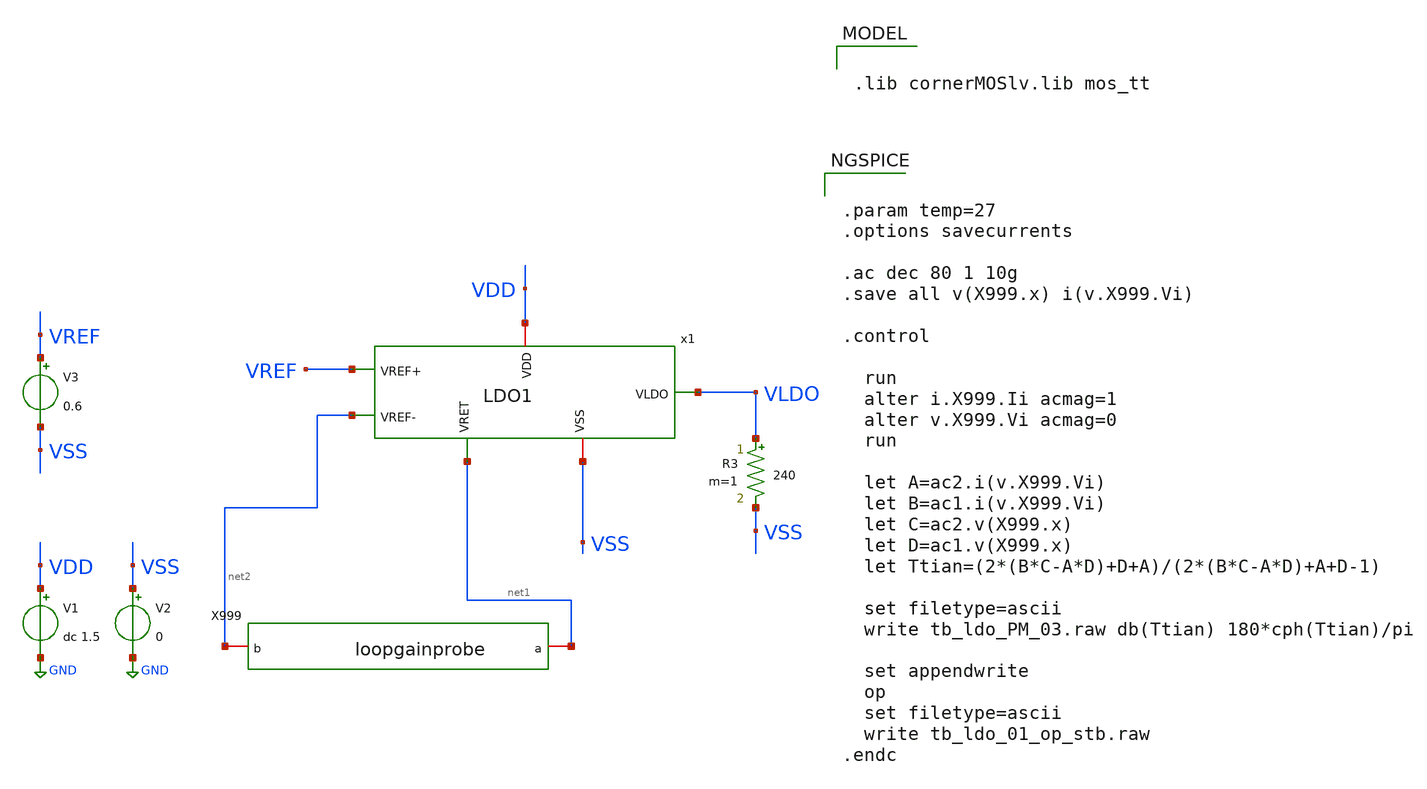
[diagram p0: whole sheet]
** sch_path: designs/1iee34/tb_ldo_PM.sch
**.subckt tb_ldo_PM
V1 VDD GND dc 1.5
V2 VSS GND 0
V3 VREF VSS 0.6
R3 VLDO VSS 240 m=1
x1 VDD VREF net2 VLDO net1 VSS LDO1
X999 net2 net1 loopgainprobe
**** begin user architecture code


.param temp=27
.options savecurrents

.ac dec 80 1 10g
.save all v(X999.x) i(v.X999.Vi)

.control

  run
  alter i.X999.Ii acmag=1
  alter v.X999.Vi acmag=0
  run

  let A=ac2.i(v.X999.Vi)
  let B=ac1.i(v.X999.Vi)
  let C=ac2.v(X999.x)
  let D=ac1.v(X999.x)
  let Ttian=(2*(B*C-A*D)+D+A)/(2*(B*C-A*D)+A+D-1)

  set filetype=ascii
  write tb_ldo_PM_03.raw db(Ttian) 180*cph(Ttian)/pi

  set appendwrite
  op
  set filetype=ascii
  write tb_ldo_01_op_stb.raw
.endc




.lib cornerMOSlv.lib mos_tt


**** end user architecture code
**.ends

* expanding   symbol:  LDO1.sym # of pins=6
** sym_path: designs/1iee34/LDO1.sym
** sch_path: designs/1iee34/LDO1.sch
.subckt LDO1 VDD VREF+ VREF- VLDO VRET VSS
*.iopin VREF+
*.iopin VLDO
*.iopin VDD
*.iopin VREF-
*.iopin VSS
*.iopin VRET
C1 VLDO VSS 1000.0n m=1
CC net4 net1 3.666349378452877e-05n m=1
R1 VLDO VRET 21.49k m=1
R2 VRET VSS 21.49k m=1
C3 VLDO net5 5n m=1
R3 net1 net5 30k m=1
XMG VLDO net1 VDD VDD sg13_lv_pmos w=250.0u l=0.13u ng=13 m=1 mm_ok=1
XM3 net3 net3 VDD VDD sg13_lv_pmos w=14.74u l=32.58u ng=2 m=1 mm_ok=1
XM4 net4 net3 VDD VDD sg13_lv_pmos w=14.74u l=32.58u ng=2 m=1 mm_ok=1
XM6 net1 net4 VDD VDD sg13_lv_pmos w=3.58u l=1.5u ng=1 m=1 mm_ok=1
XM1 net2 VREF+ net3 VSS sg13_lv_nmos w=176.34u l=8.55u ng=18 m=1 mm_ok=1
XM2 net2 VREF- net4 VSS sg13_lv_nmos w=176.34u l=8.55u ng=18 m=1 mm_ok=1
XM5 VSS VG net2 VSS sg13_lv_nmos w=2.2u l=2.0u ng=1 m=1 mm_ok=1
XM7 VSS VG net1 VSS sg13_lv_nmos w=4.4u l=2.0u ng=1 m=1 mm_ok=1
XM8 VSS VG VG VSS sg13_lv_nmos w=2.75u l=2.0u ng=1 m=1 mm_ok=1
XM10 net6 net6 VDD VDD sg13_lv_pmos w=2u l=8u ng=1 m=1 mm_ok=1
XM11 VG VDD net6 VSS sg13_lv_nmos w=2u l=8u ng=1 m=1 mm_ok=1
.ends


* expanding   symbol:  loopgainprobe.sym # of pins=2
** sym_path: designs/1iee34/loopgainprobe.sym
** sch_path: designs/1iee34/loopgainprobe.sch
.subckt loopgainprobe b a
*.iopin a
*.iopin b
Vi x a dc 0 ac 1
Ii GND x dc 0 ac 0
Vnodebuffer b x 0
.ends

.GLOBAL GND
.end
